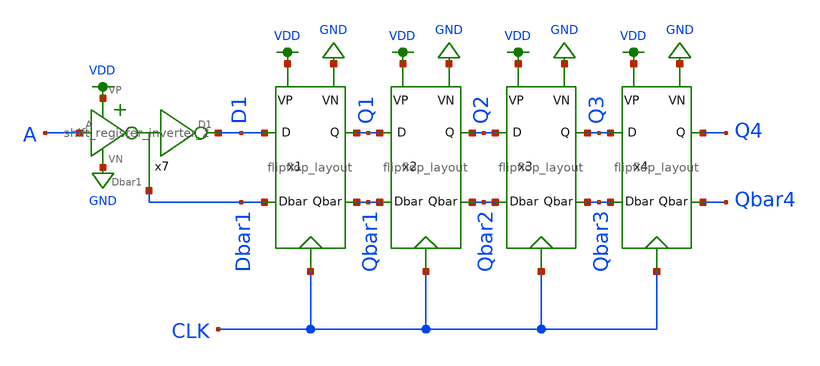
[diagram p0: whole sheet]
** sch_path: mp2/submission/LVS/shift_register_lvs.sch
**.subckt shift_register_lvs
x1 D1 VDD Dbar1 GND Q1 CLK Qbar1 flipflop_layout
x2 Q1 VDD Qbar1 GND Q2 CLK Qbar2 flipflop_layout
x3 Q2 VDD Qbar2 GND Q3 CLK Qbar3 flipflop_layout
x4 Q3 VDD Qbar3 GND Q4 CLK Qbar4 flipflop_layout
x7 VDD A D1 Dbar1 GND shift_register_inverter_2
**.ends
.GLOBAL GND
.GLOBAL VDD
.end
